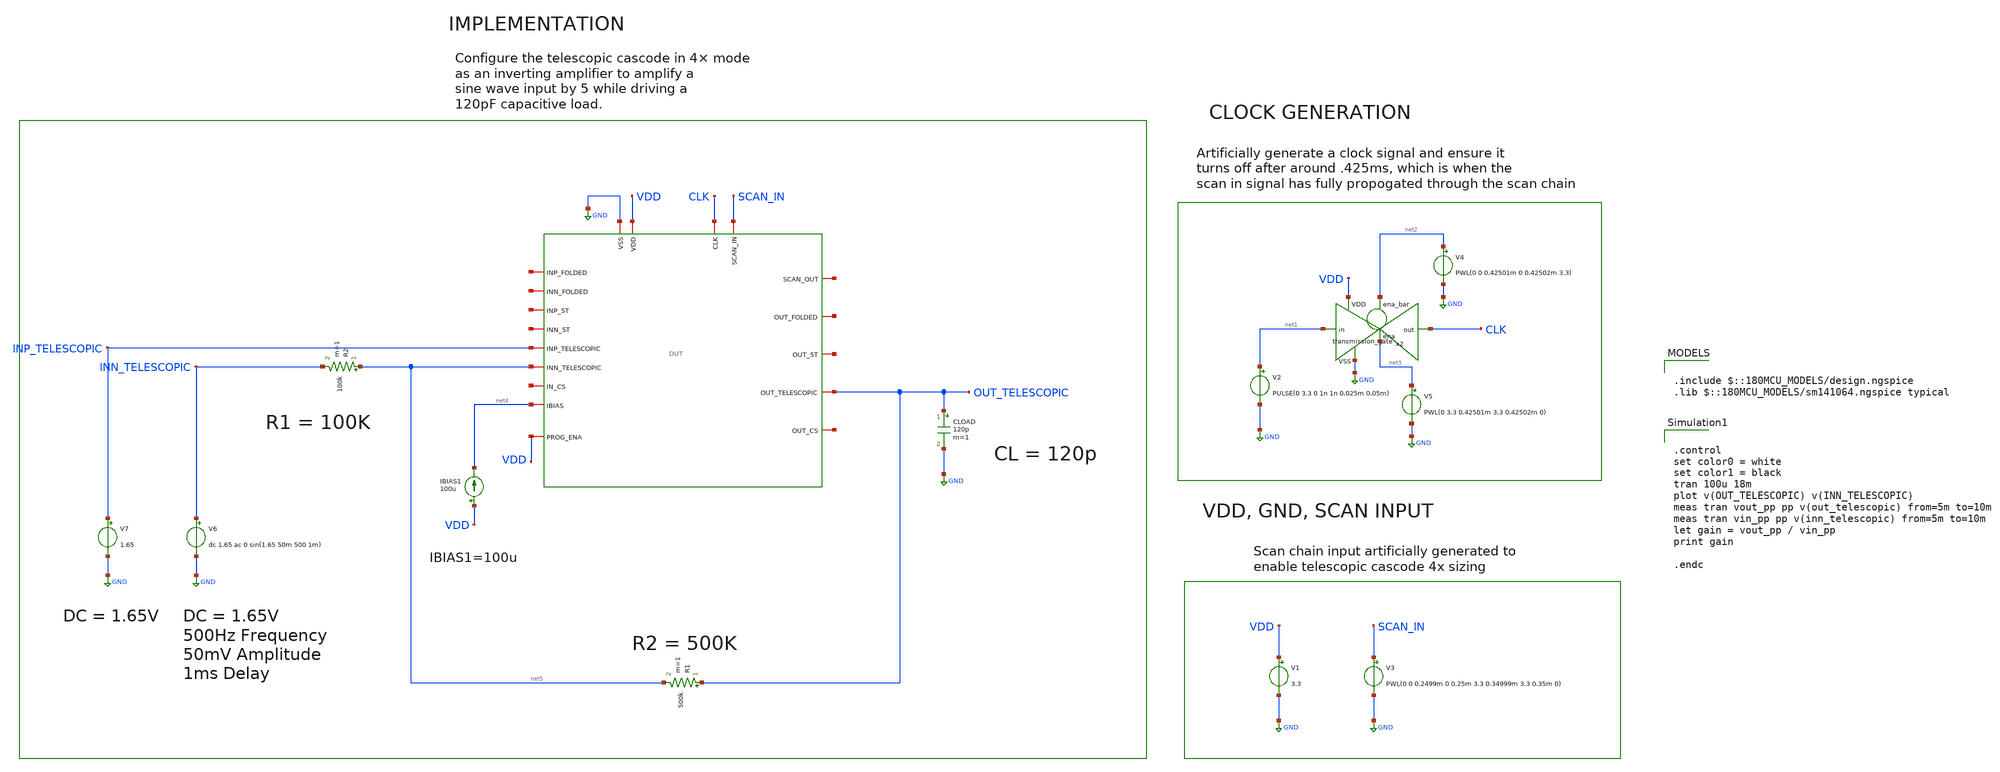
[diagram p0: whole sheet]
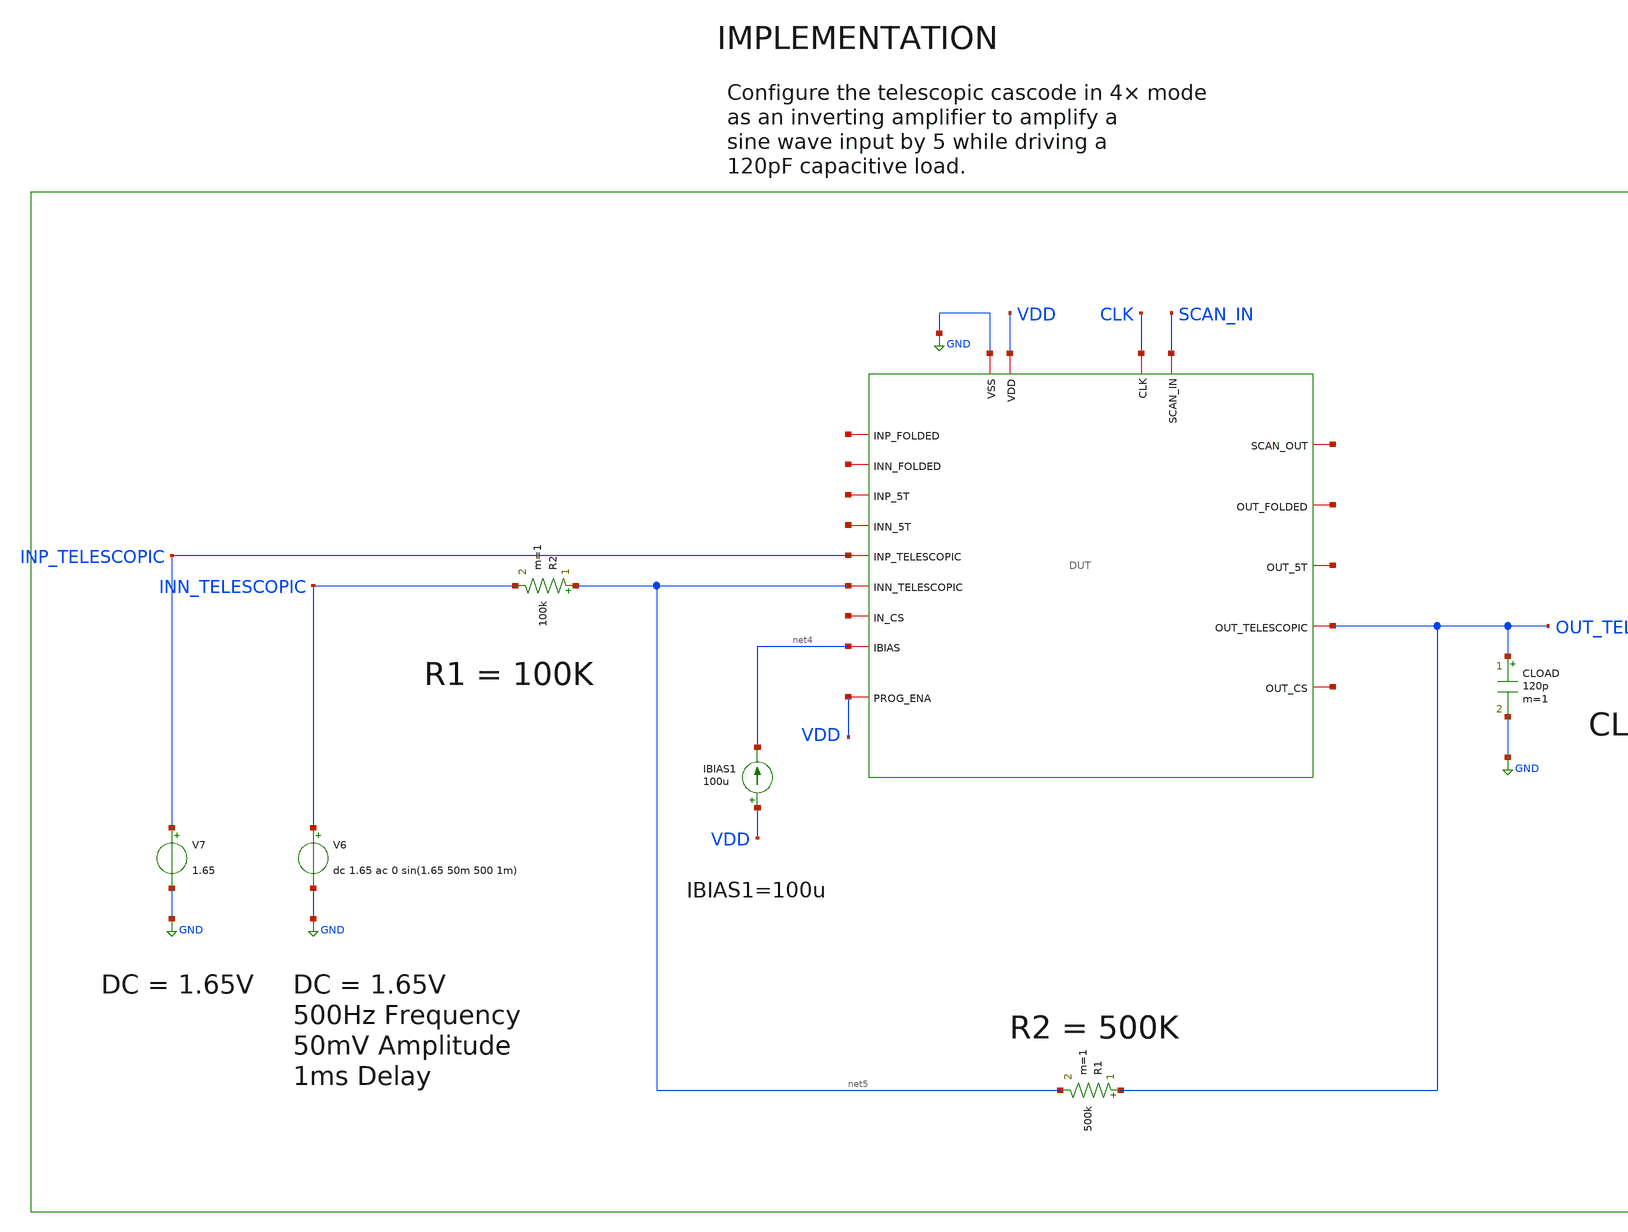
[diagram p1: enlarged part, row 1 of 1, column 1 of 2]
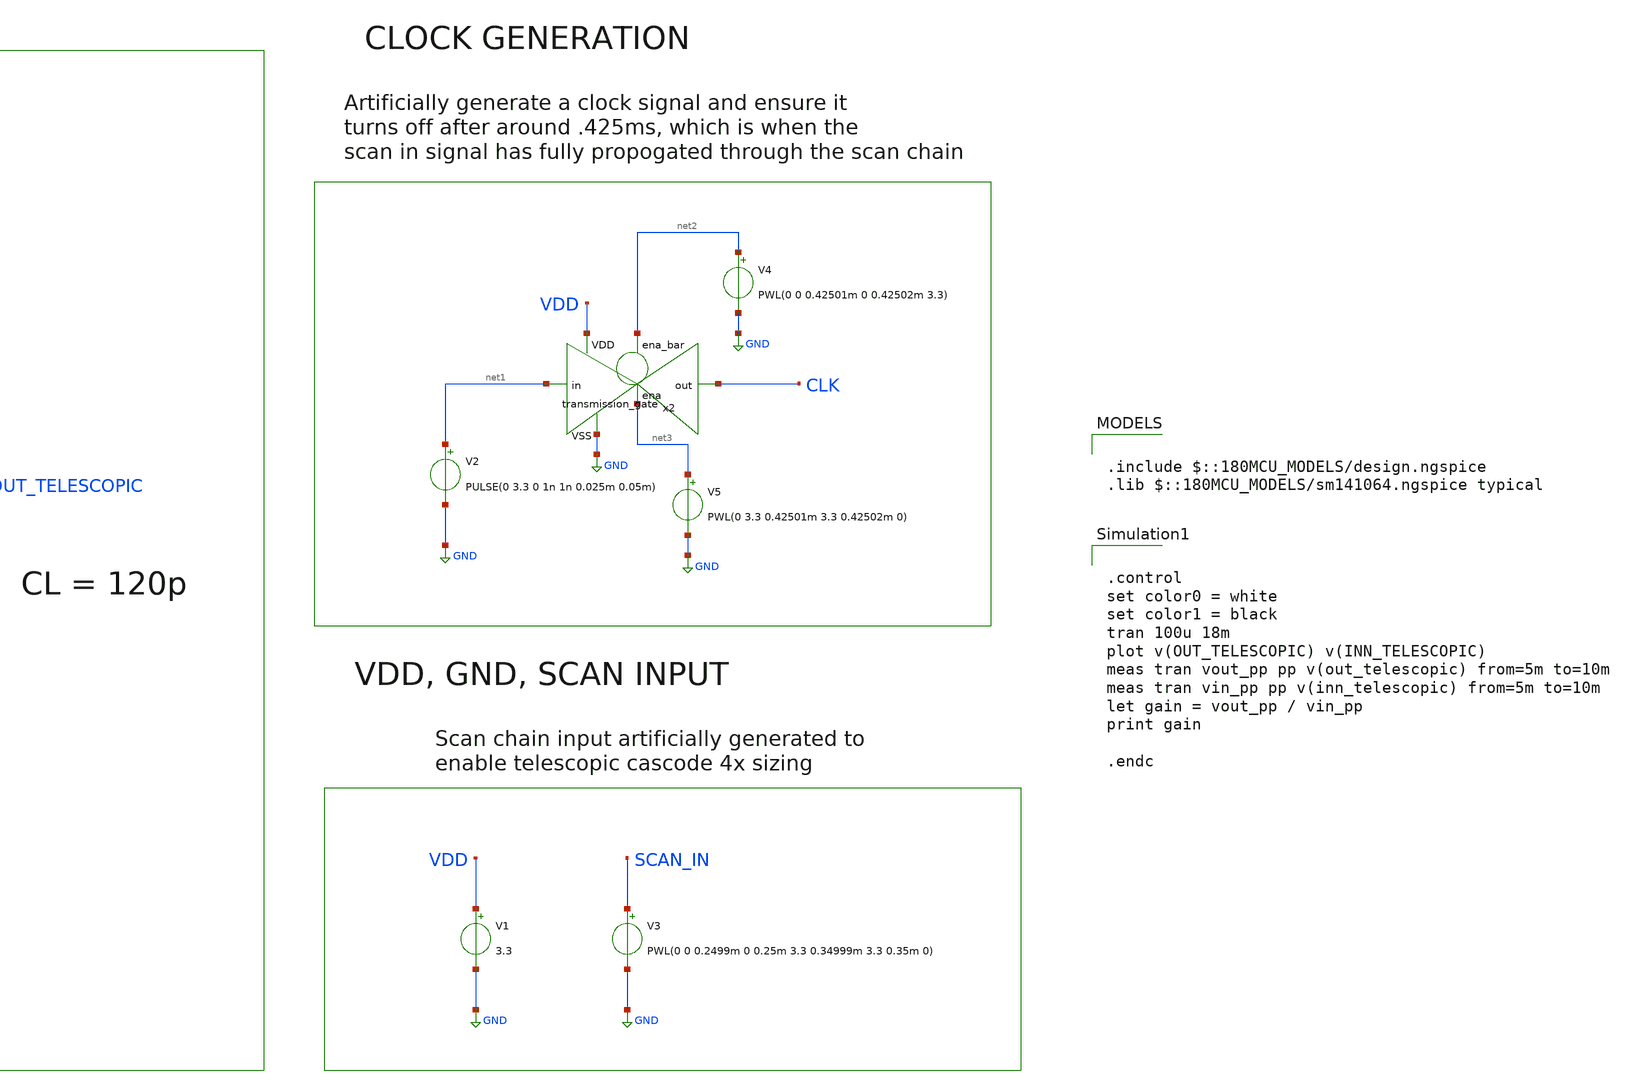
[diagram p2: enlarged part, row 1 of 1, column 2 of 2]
** sch_path: designs/libs/core_tb/mpg/ota_telescopic/Inverting/telescopic_4x_5x.sch
**.subckt telescopic_4x_5x
V3 SCAN_IN GND PWL(0 0 0.2499m 0 0.25m 3.3 0.34999m 3.3 0.35m 0)
V1 VDD GND 3.3
V2 net1 GND PULSE(0 3.3 0 1n 1n 0.025m 0.05m)
x2 net2 VDD CLK net1 GND net3 transmission_gate
V4 net2 GND PWL(0 0 0.42501m 0 0.42502m 3.3)
V5 net3 GND PWL(0 3.3 0.42501m 3.3 0.42502m 0)
IBIAS1 VDD net4 100u
V7 INP_TELESCOPIC GND 1.65
CLOAD OUT_TELESCOPIC GND 120p m=1
R2 net5 INN_TELESCOPIC 100k m=1
V6 INN_TELESCOPIC GND dc 1.65 ac 0 sin(1.65 50m 500 1m)
R1 OUT_TELESCOPIC net5 500k m=1
x1 CLK net6 SCAN_IN GND VDD net7 net8 net9 net4 net10 net11 net12 INP_TELESCOPIC OUT_TELESCOPIC
+ net13 net14 net5 VDD DUT
**** begin user architecture code

.include $::180MCU_MODELS/design.ngspice
.lib $::180MCU_MODELS/sm141064.ngspice typical



.control
set color0 = white
set color1 = black
tran 100u 18m
plot v(OUT_TELESCOPIC) v(INN_TELESCOPIC)
meas tran vout_pp pp v(out_telescopic) from=5m to=10m
meas tran vin_pp pp v(inn_telescopic) from=5m to=10m
let gain = vout_pp / vin_pp
print gain

.endc


**** end user architecture code
**.ends
.GLOBAL GND
.end
